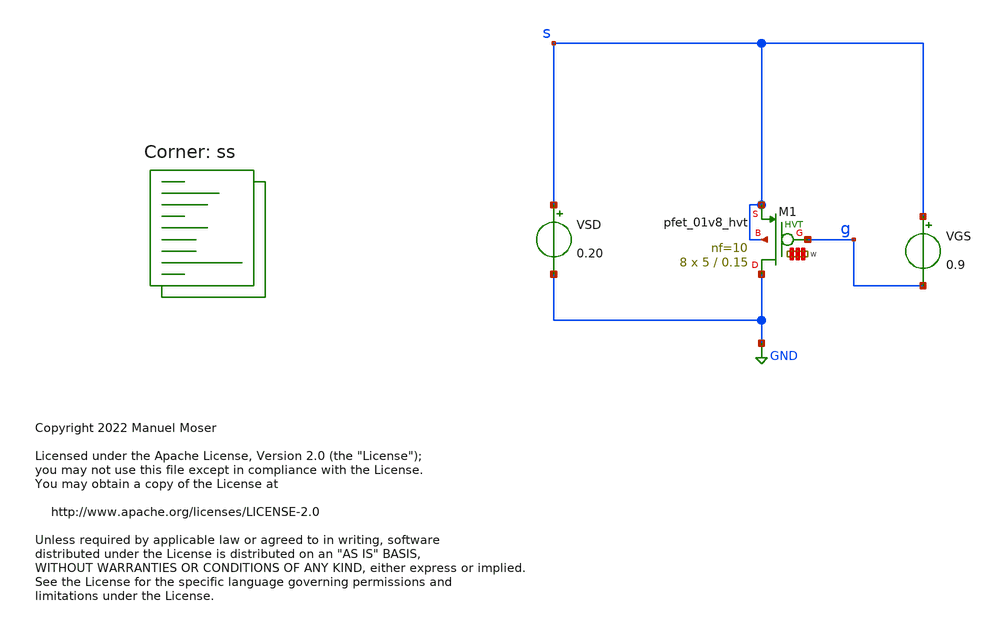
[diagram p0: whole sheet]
** sch_path: xschem/ldo_pmos_eval.sch
* Copyright 2022 Manuel Moser
* Licensed under the Apache License, Version 2.0 (the "License");
**.subckt ldo_pmos_eval
XM1 GND g s s sky130_fd_pr__pfet_01v8_hvt L=0.15 W='5 * 10 ' nf=10 ad='int((nf+1)/2) * W / nf * 0.29'
+ as='int((nf+2)/2) * W / nf * 0.29' pd='2*int((nf+1)/2) * (W / nf + 0.29)' ps='2*int((nf+2)/2) * (W / nf + 0.29)'
+ nrd='0.29 / W ' nrs='0.29 / W ' sa=0 sb=0 sd=0 mult=8 m=8
VSD s GND 0.20
VGS s g 0.9
**** begin user architecture code



.temp 27

.save all
.save @m.xm1.msky130_fd_pr__pfet_01v8_lvt[Vth]
.save @m.xm1.msky130_fd_pr__pfet_01v8_lvt[gm]

.control
set num_threads=12
dc VGS 0 1.8 0.1
plot (-i(vsd))
plot @m.xm1.msky130_fd_pr__pfet_01v8_lvt[gm]

op
write pmos_power_transistor_tb.raw
print v(@m.xm1.msky130_fd_pr__pfet_01v8_lvt[Vth])

.endc



.lib $::SKYWATER_MODELS/sky130.lib.spice ss
**** end user architecture code
**.ends
.GLOBAL GND
.end
